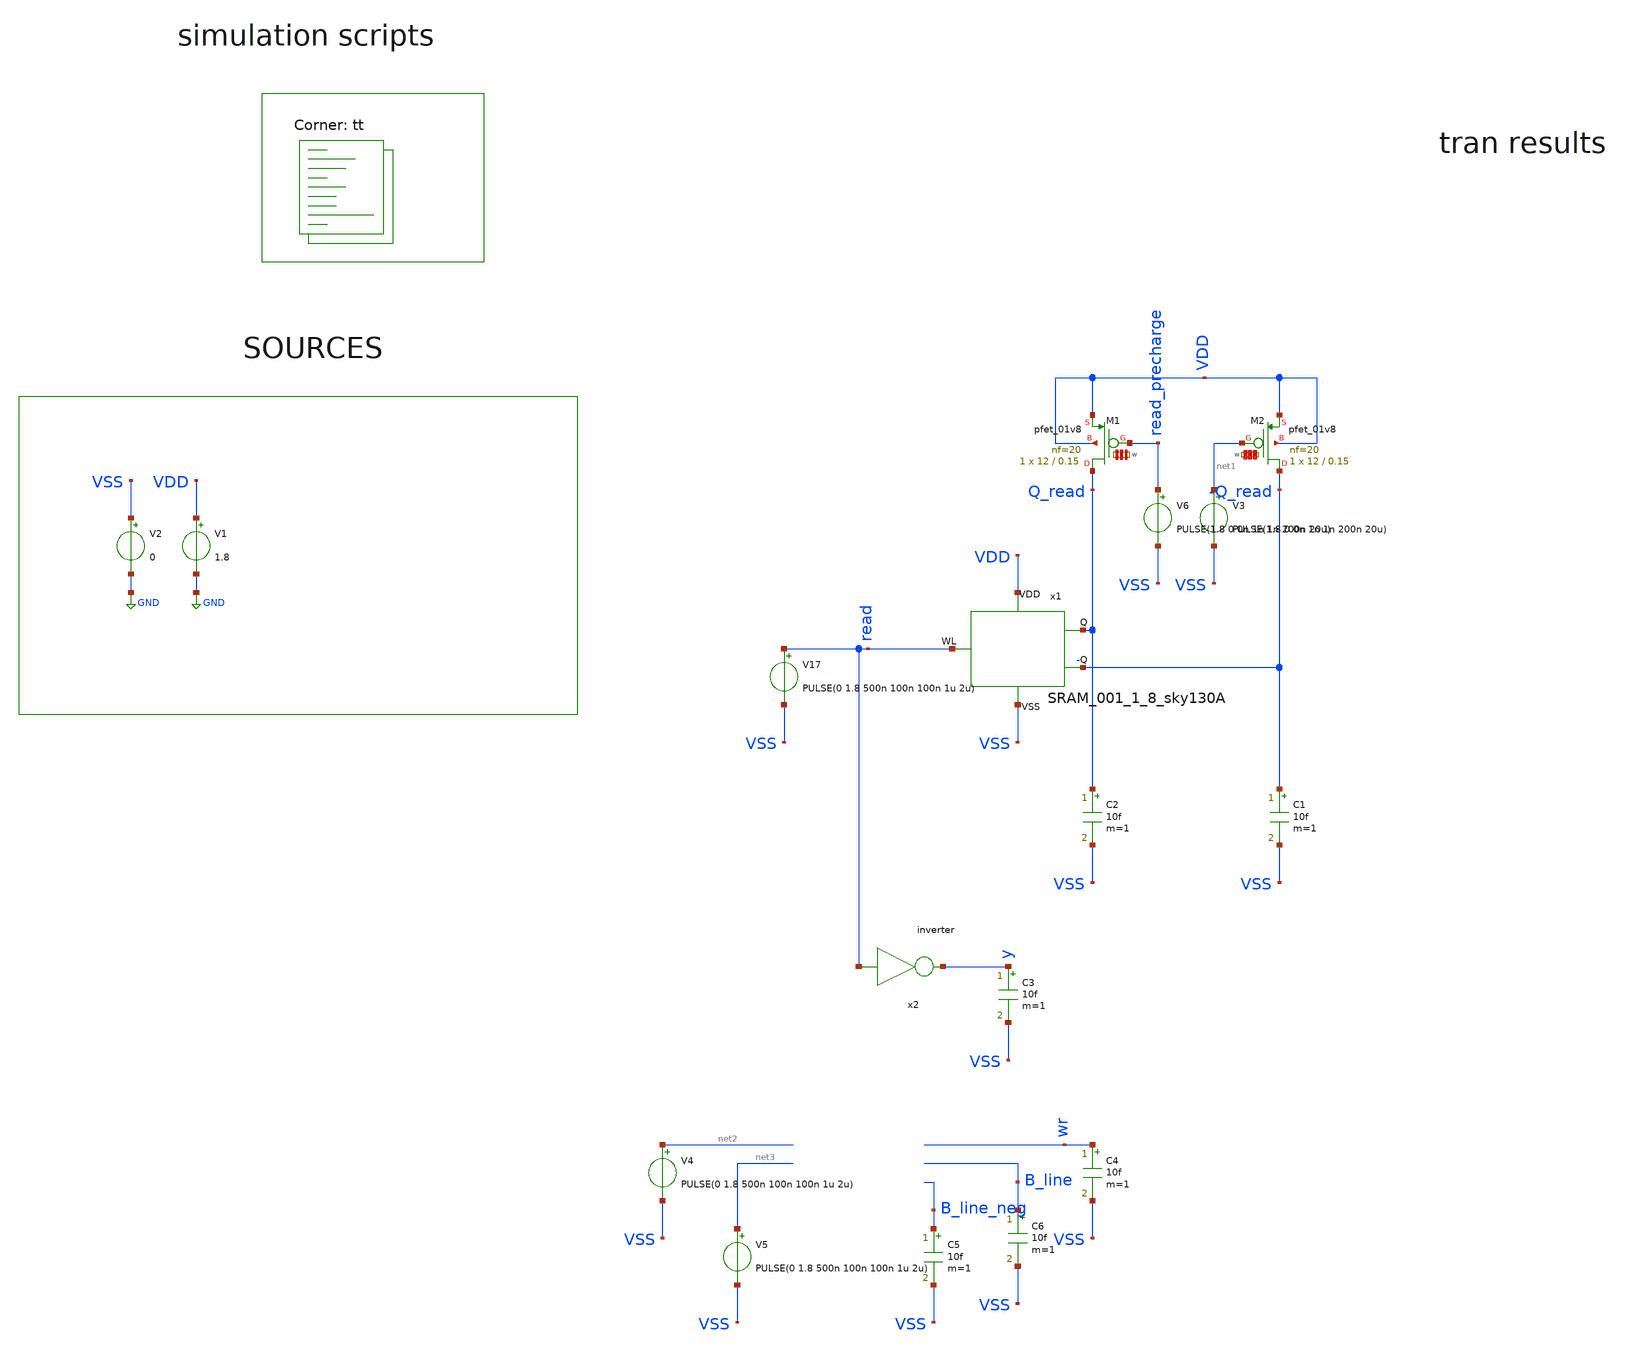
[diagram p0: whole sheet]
** sch_path: my_ip/sky130A/Memory_tb/tb.sch
**.subckt tb
V1 VDD GND 1.8
V2 VSS GND 0
V17 read VSS PULSE(0 1.8 500n 100n 100n 1u 2u)
x1 VDD VSS read Q_read -Q_read SRAM_001_1_8_sky130A
V6 read_precharge VSS PULSE(1.8 0 0n 1n 1n 200n 20u)
XM2 -Q_read net1 VDD VDD sky130_fd_pr__pfet_01v8 L=0.15 W='12 * 20 ' nf=20 ad= as='int((20 + 2)/2) * 12 * 0.29'
+ pd='2*int((20 + 1)/2) * (12 + 0.29)' ps='2*int((20 + 2)/2) * (12 + 0.29)' nrd='0.29 / 12 / 20 ' nrs='0.29 / 12 / 20 '
+ sa=0 sb=0 sd=0 mult=1 m=1
XM1 Q_read read_precharge VDD VDD sky130_fd_pr__pfet_01v8 L=0.15 W='12 * 20 ' nf=20 ad= as='int((20 + 2)/2) * 12 * 0.29'
+ pd='2*int((20 + 1)/2) * (12 + 0.29)' ps='2*int((20 + 2)/2) * (12 + 0.29)' nrd='0.29 / 12 / 20 ' nrs='0.29 / 12 / 20 '
+ sa=0 sb=0 sd=0 mult=1 m=1
V3 net1 VSS PULSE(1.8 0 0n 1n 1n 200n 20u)
C1 -Q_read VSS 10f m=1
C2 Q_read VSS 10f m=1
C3 y VSS 10f m=1
V4 net2 VSS PULSE(0 1.8 500n 100n 100n 1u 2u)
C4 wr VSS 10f m=1
C5 B_line_neg VSS 10f m=1
C6 B_line VSS 10f m=1
V5 net3 VSS PULSE(0 1.8 500n 100n 100n 1u 2u)
x2 read VGND VNB VPB VPWR y
**** begin user architecture code
.lib $::SKYWATER_MODELS/sky130.lib.spice tt

**************************************************************
**************************************************************
**************************************************************
**************************************************************
**************************************************************
*LIBs*********************************************************
**************************************************************
**************************************************************
**************************************************************
**************************************************************
**************************************************************
*.lib $::SKYWATER_MODELS/sky130.lib.spice tt
* chose the corners in the corner file
* tt_mm for mismatch
* ss ff sf fs standart corners
* ll hh lh hl capacitor and resistors corners
* mc for total process variation including corners
**************************************************************
**************************************************************
**************************************************************
**************************************************************
**************************************************************
*Corners/montecarlo options***********************************
**************************************************************
**************************************************************
**************************************************************
**************************************************************
**************************************************************
.TEMP 27
**************************************************************
**************************************************************
**************************************************************
**************************************************************
*SIMULATION and Plots*****************************************
**************************************************************
**************************************************************
**************************************************************
**************************************************************
.include ~/PDK/sky130A/libs.ref/sky130_fd_sc_hd/spice/sky130_fd_sc_hd.spice

.include /home/vasco/Desktop/OSAD/my_ip/LIB/digital/inverter.spice

VVPWR VPWR 0 1.8
VVGND VGND 0 0
VVNB VNB 0 0
VVPB VPB 0 1.8

.control
save all
op
write tb.raw
set appendwrite

tran 1ns 100u
set appendwrite
write tb.raw

.endc

**** end user architecture code
**.ends

* expanding   symbol:  Memory/SRAM_001_1_8_sky130A.sym # of pins=5
** sym_path: my_ip/LIB/Memory/SRAM_001_1_8_sky130A.sym
** sch_path: my_ip/LIB/Memory/SRAM_001_1_8_sky130A.sch
.subckt SRAM_001_1_8_sky130A VDD VSS WL Q -Q
*.iopin VDD
*.iopin VSS
*.iopin WL
*.iopin Q
*.iopin -Q
XM1 a b VDD VDD sky130_fd_pr__pfet_01v8 L=0.15 W='2 * 6 ' nf=6 ad= as='int((6 + 2)/2) * 2 * 0.29' pd='2*int((6 + 1)/2) * (2 + 0.29)'
+ ps='2*int((6 + 2)/2) * (2 + 0.29)' nrd='0.29 / 2 / 6 ' nrs='0.29 / 2 / 6 ' sa=0 sb=0 sd=0 mult=2 m=2
XM2 a b VSS VSS sky130_fd_pr__nfet_01v8_lvt L=0.15 W='2 * 2 ' nf=2 ad='int((2 + 1)/2) * 2 / 2 * 0.29'
+ as='int((2 + 2)/2) * 2 / 2 * 0.29' pd='2*int((2 + 1)/2) * (2 / 2 + 0.29)' ps='2*int((2 + 2)/2) * (2 / 2 + 0.29)'
+ nrd='0.29 / 2 ' nrs='0.29 / 2 ' sa=0 sb=0 sd=0 mult=2 m=2
XM3 b a VSS VSS sky130_fd_pr__nfet_01v8_lvt L=0.15 W='2 * 2 ' nf=2 ad='int((2 + 1)/2) * 2 / 2 * 0.29'
+ as='int((2 + 2)/2) * 2 / 2 * 0.29' pd='2*int((2 + 1)/2) * (2 / 2 + 0.29)' ps='2*int((2 + 2)/2) * (2 / 2 + 0.29)'
+ nrd='0.29 / 2 ' nrs='0.29 / 2 ' sa=0 sb=0 sd=0 mult=2 m=2
XM4 b a VDD VDD sky130_fd_pr__pfet_01v8 L=0.15 W='2 * 6 ' nf=6 ad= as='int((6 + 2)/2) * 2 * 0.29' pd='2*int((6 + 1)/2) * (2 + 0.29)'
+ ps='2*int((6 + 2)/2) * (2 + 0.29)' nrd='0.29 / 2 / 6 ' nrs='0.29 / 2 / 6 ' sa=0 sb=0 sd=0 mult=2 m=2
XM5 Q WL a VSS sky130_fd_pr__nfet_01v8_lvt L=0.15 W='1 * 2 ' nf=2 ad='int((2 + 1)/2) * 1 / 2 * 0.29'
+ as='int((2 + 2)/2) * 1 / 2 * 0.29' pd='2*int((2 + 1)/2) * (1 / 2 + 0.29)' ps='2*int((2 + 2)/2) * (1 / 2 + 0.29)'
+ nrd='0.29 / 1 ' nrs='0.29 / 1 ' sa=0 sb=0 sd=0 mult=1 m=1
XM6 -Q WL b VSS sky130_fd_pr__nfet_01v8_lvt L=0.15 W='1 * 2 ' nf=2 ad='int((2 + 1)/2) * 1 / 2 * 0.29'
+ as='int((2 + 2)/2) * 1 / 2 * 0.29' pd='2*int((2 + 1)/2) * (1 / 2 + 0.29)' ps='2*int((2 + 2)/2) * (1 / 2 + 0.29)'
+ nrd='0.29 / 1 ' nrs='0.29 / 1 ' sa=0 sb=0 sd=0 mult=1 m=1
.ends

.GLOBAL GND
.end
